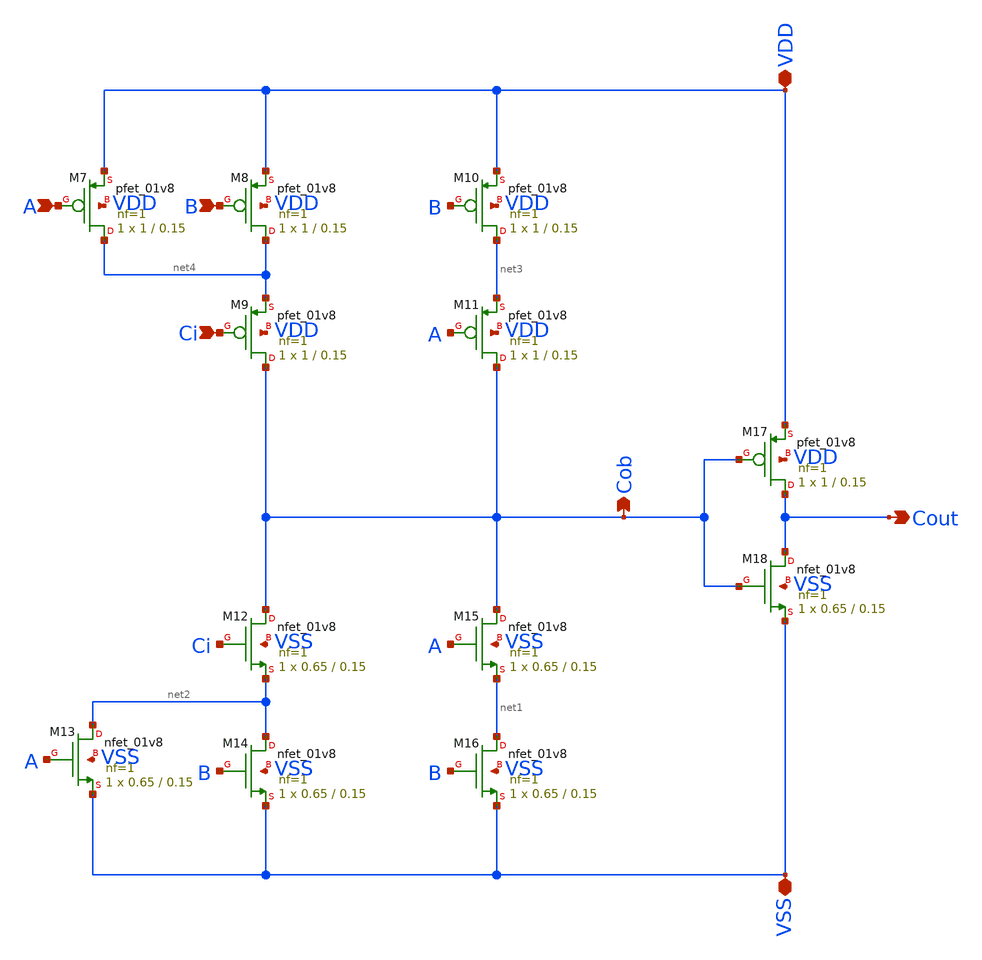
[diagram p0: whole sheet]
** sch_path: xschem/carry.sch
**.subckt carry VDD VSS Cout Cob A B Ci
*.iopin VDD
*.iopin VSS
*.opin Cout
*.opin Cob
*.ipin A
*.ipin B
*.ipin Ci
XM7 net4 A VDD VDD sky130_fd_pr__pfet_01v8 L=0.15 W=1 nf=1 ad='int((1 + 1)/2) * 1 / 1 * 0.29' as='int((1 + 2)/2) * 1 / 1 * 0.29'
+ pd='2*int((1 + 1)/2) * (1 / 1 + 0.29)' ps='2*int((1 + 2)/2) * (1 / 1 + 0.29)' nrd='0.29 / 1 ' nrs='0.29 / 1 '
+ sa=0 sb=0 sd=0 mult=1 m=1
XM8 net4 B VDD VDD sky130_fd_pr__pfet_01v8 L=0.15 W=1 nf=1 ad='int((1 + 1)/2) * 1 / 1 * 0.29' as='int((1 + 2)/2) * 1 / 1 * 0.29'
+ pd='2*int((1 + 1)/2) * (1 / 1 + 0.29)' ps='2*int((1 + 2)/2) * (1 / 1 + 0.29)' nrd='0.29 / 1 ' nrs='0.29 / 1 '
+ sa=0 sb=0 sd=0 mult=1 m=1
XM9 Cob Ci net4 VDD sky130_fd_pr__pfet_01v8 L=0.15 W=1 nf=1 ad='int((1 + 1)/2) * 1 / 1 * 0.29' as='int((1 + 2)/2) * 1 / 1 * 0.29'
+ pd='2*int((1 + 1)/2) * (1 / 1 + 0.29)' ps='2*int((1 + 2)/2) * (1 / 1 + 0.29)' nrd='0.29 / 1 ' nrs='0.29 / 1 '
+ sa=0 sb=0 sd=0 mult=1 m=1
XM10 net3 B VDD VDD sky130_fd_pr__pfet_01v8 L=0.15 W=1 nf=1 ad='int((1 + 1)/2) * 1 / 1 * 0.29' as='int((1 + 2)/2) * 1 / 1 * 0.29'
+ pd='2*int((1 + 1)/2) * (1 / 1 + 0.29)' ps='2*int((1 + 2)/2) * (1 / 1 + 0.29)' nrd='0.29 / 1 ' nrs='0.29 / 1 '
+ sa=0 sb=0 sd=0 mult=1 m=1
XM11 Cob A net3 VDD sky130_fd_pr__pfet_01v8 L=0.15 W=1 nf=1 ad='int((1 + 1)/2) * 1 / 1 * 0.29' as='int((1 + 2)/2) * 1 / 1 * 0.29'
+ pd='2*int((1 + 1)/2) * (1 / 1 + 0.29)' ps='2*int((1 + 2)/2) * (1 / 1 + 0.29)' nrd='0.29 / 1 ' nrs='0.29 / 1 '
+ sa=0 sb=0 sd=0 mult=1 m=1
XM12 Cob Ci net2 VSS sky130_fd_pr__nfet_01v8 L=0.15 W=0.65 nf=1 ad='int((1 + 1)/2) * 0.65 / 1 * 0.29'
+ as='int((1 + 2)/2) * 0.65 / 1 * 0.29' pd='2*int((1 + 1)/2) * (0.65 / 1 + 0.29)' ps='2*int((1 + 2)/2) * (0.65 / 1 + 0.29)'
+ nrd='0.29 / 0.65 ' nrs='0.29 / 0.65 ' sa=0 sb=0 sd=0 mult=1 m=1
XM13 net2 A VSS VSS sky130_fd_pr__nfet_01v8 L=0.15 W=0.65 nf=1 ad='int((1 + 1)/2) * 0.65 / 1 * 0.29'
+ as='int((1 + 2)/2) * 0.65 / 1 * 0.29' pd='2*int((1 + 1)/2) * (0.65 / 1 + 0.29)' ps='2*int((1 + 2)/2) * (0.65 / 1 + 0.29)'
+ nrd='0.29 / 0.65 ' nrs='0.29 / 0.65 ' sa=0 sb=0 sd=0 mult=1 m=1
XM14 net2 B VSS VSS sky130_fd_pr__nfet_01v8 L=0.15 W=0.65 nf=1 ad='int((1 + 1)/2) * 0.65 / 1 * 0.29'
+ as='int((1 + 2)/2) * 0.65 / 1 * 0.29' pd='2*int((1 + 1)/2) * (0.65 / 1 + 0.29)' ps='2*int((1 + 2)/2) * (0.65 / 1 + 0.29)'
+ nrd='0.29 / 0.65 ' nrs='0.29 / 0.65 ' sa=0 sb=0 sd=0 mult=1 m=1
XM15 Cob A net1 VSS sky130_fd_pr__nfet_01v8 L=0.15 W=0.65 nf=1 ad='int((1 + 1)/2) * 0.65 / 1 * 0.29'
+ as='int((1 + 2)/2) * 0.65 / 1 * 0.29' pd='2*int((1 + 1)/2) * (0.65 / 1 + 0.29)' ps='2*int((1 + 2)/2) * (0.65 / 1 + 0.29)'
+ nrd='0.29 / 0.65 ' nrs='0.29 / 0.65 ' sa=0 sb=0 sd=0 mult=1 m=1
XM16 net1 B VSS VSS sky130_fd_pr__nfet_01v8 L=0.15 W=0.65 nf=1 ad='int((1 + 1)/2) * 0.65 / 1 * 0.29'
+ as='int((1 + 2)/2) * 0.65 / 1 * 0.29' pd='2*int((1 + 1)/2) * (0.65 / 1 + 0.29)' ps='2*int((1 + 2)/2) * (0.65 / 1 + 0.29)'
+ nrd='0.29 / 0.65 ' nrs='0.29 / 0.65 ' sa=0 sb=0 sd=0 mult=1 m=1
XM17 Cout Cob VDD VDD sky130_fd_pr__pfet_01v8 L=0.15 W=1 nf=1 ad='int((1 + 1)/2) * 1 / 1 * 0.29' as='int((1 + 2)/2) * 1 / 1 * 0.29'
+ pd='2*int((1 + 1)/2) * (1 / 1 + 0.29)' ps='2*int((1 + 2)/2) * (1 / 1 + 0.29)' nrd='0.29 / 1 ' nrs='0.29 / 1 '
+ sa=0 sb=0 sd=0 mult=1 m=1
XM18 Cout Cob VSS VSS sky130_fd_pr__nfet_01v8 L=0.15 W=0.65 nf=1 ad='int((1 + 1)/2) * 0.65 / 1 * 0.29'
+ as='int((1 + 2)/2) * 0.65 / 1 * 0.29' pd='2*int((1 + 1)/2) * (0.65 / 1 + 0.29)' ps='2*int((1 + 2)/2) * (0.65 / 1 + 0.29)'
+ nrd='0.29 / 0.65 ' nrs='0.29 / 0.65 ' sa=0 sb=0 sd=0 mult=1 m=1
**.ends
.end
